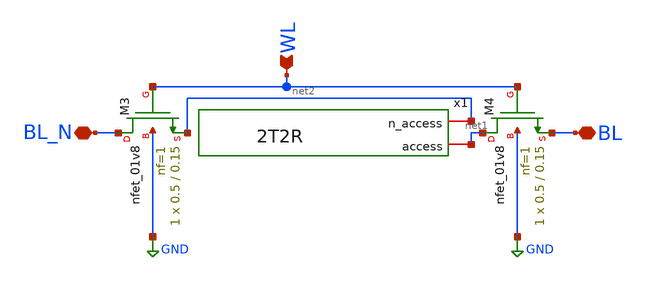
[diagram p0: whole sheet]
** sch_path: analog/schematics/Access_2T2R.sch
**.subckt Access_2T2R BL_N BL WL
*.iopin BL_N
*.iopin BL
*.ipin WL
XM3 BL_N WL net2 GND sky130_fd_pr__nfet_01v8 L=0.15 W=0.5 nf=1 ad='int((nf+1)/2) * W/nf * 0.29' as='int((nf+2)/2) * W/nf * 0.29'
+ pd='2*int((nf+1)/2) * (W/nf + 0.29)' ps='2*int((nf+2)/2) * (W/nf + 0.29)' nrd='0.29 / W' nrs='0.29 / W'
+ sa=0 sb=0 sd=0 mult=1 m=1
XM4 net1 WL BL GND sky130_fd_pr__nfet_01v8 L=0.15 W=0.5 nf=1 ad='int((nf+1)/2) * W/nf * 0.29' as='int((nf+2)/2) * W/nf * 0.29'
+ pd='2*int((nf+1)/2) * (W/nf + 0.29)' ps='2*int((nf+2)/2) * (W/nf + 0.29)' nrd='0.29 / W' nrs='0.29 / W'
+ sa=0 sb=0 sd=0 mult=1 m=1
x1 net2 net1 2T2R
**.ends
.GLOBAL GND
.end
